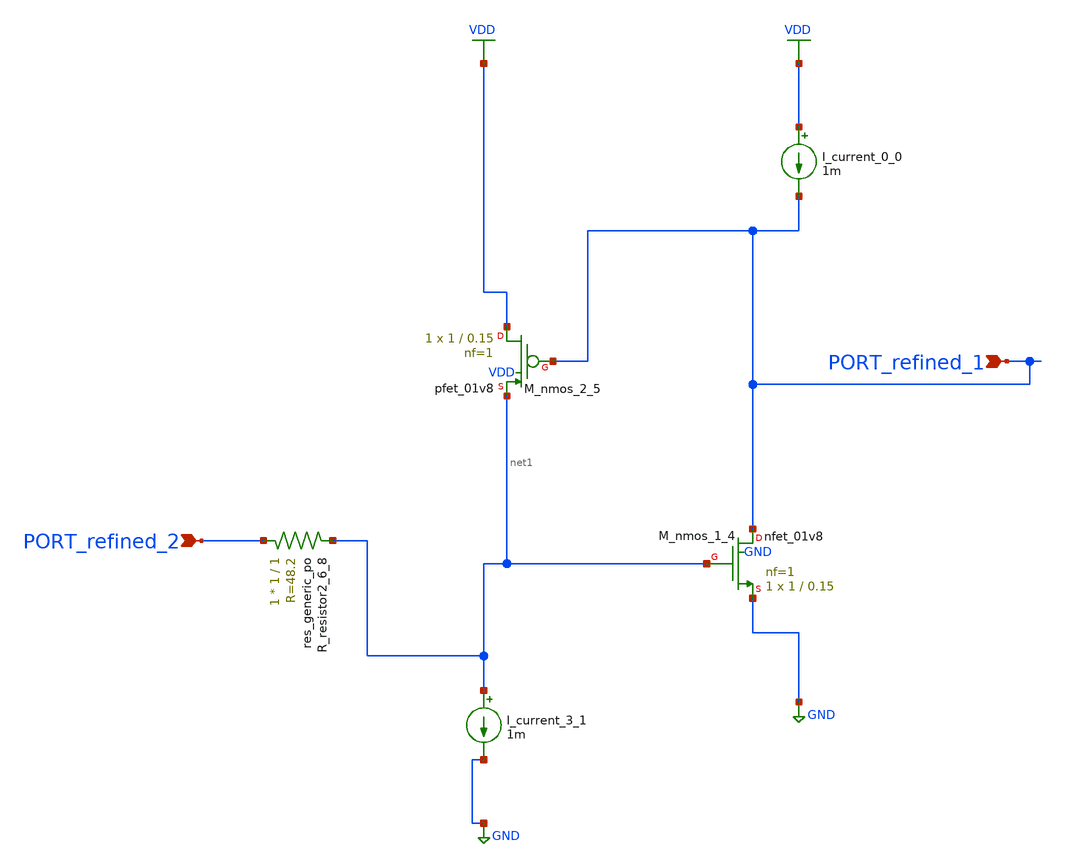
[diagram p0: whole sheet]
** sch_path: schematics/AMSNet/411.sch
**.subckt 411 PORT_refined_1 PORT_refined_2
*.ipin PORT_refined_1
*.ipin PORT_refined_2
I_current_0_0 VDD PORT_refined_1 1m
I_current_3_1 net1 GND 1m
XM_nmos_1_4 PORT_refined_1 net1 GND GND sky130_fd_pr__nfet_01v8 L=0.15 W=1 nf=1 ad='int((1 + 1)/2) * 1 / 1 * 0.29'
+ as='int((1 + 2)/2) * 1 / 1 * 0.29' pd='2*int((1 + 1)/2) * (1 / 1 + 0.29)' ps='2*int((1 + 2)/2) * (1 / 1 + 0.29)'
+ nrd='0.29 / 1 ' nrs='0.29 / 1 ' sa=0 sb=0 sd=0 mult=1 m=1
XM_nmos_2_5 VDD PORT_refined_1 net1 VDD sky130_fd_pr__pfet_01v8 L=0.15 W=1 nf=1 ad='int((1 + 1)/2) * 1 / 1 * 0.29'
+ as='int((1 + 2)/2) * 1 / 1 * 0.29' pd='2*int((1 + 1)/2) * (1 / 1 + 0.29)' ps='2*int((1 + 2)/2) * (1 / 1 + 0.29)'
+ nrd='0.29 / 1 ' nrs='0.29 / 1 ' sa=0 sb=0 sd=0 mult=1 m=1
XR_resistor2_6_8 PORT_refined_2 net1 sky130_fd_pr__res_generic_po W=1 L=1 m=1
**.ends
.GLOBAL GND
.GLOBAL VDD
.end
